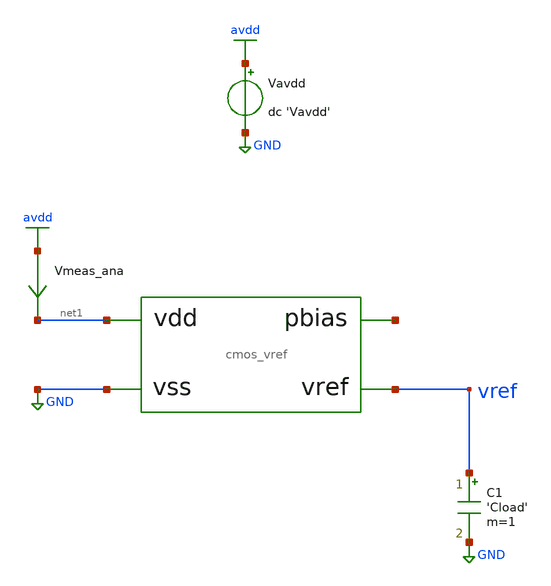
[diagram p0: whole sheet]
** sch_path: tb/cmos_vref/tb_vref_line_reg.sch
**.subckt tb_vref_line_reg
Vavdd avdd GND dc 'Vavdd'
C1 vref GND 'Cload' m=1
Vmeas_ana avdd net1 0
.save i(vmeas_ana)
X1 vref net1 GND net2 cmos_vref
**** begin user architecture code


.lib 'models_dir'/cornerMOShv.lib 'mos_corner'
.lib 'models_dir'/cornerMOSlv.lib 'mos_corner'
.lib 'models_dir'/cornerCAP.lib cap_typ
.option TEMP='temperature'
.option warn=1
.control
save vref
dc Vavdd 'vdd_min' 'vdd_max' 0.02
set wr_singlescale
wrdata 'simpath'/'filename'_'N'.data V(vref)
quit
.endc


**** end user architecture code
**.ends
.GLOBAL avdd
.GLOBAL GND
.end
